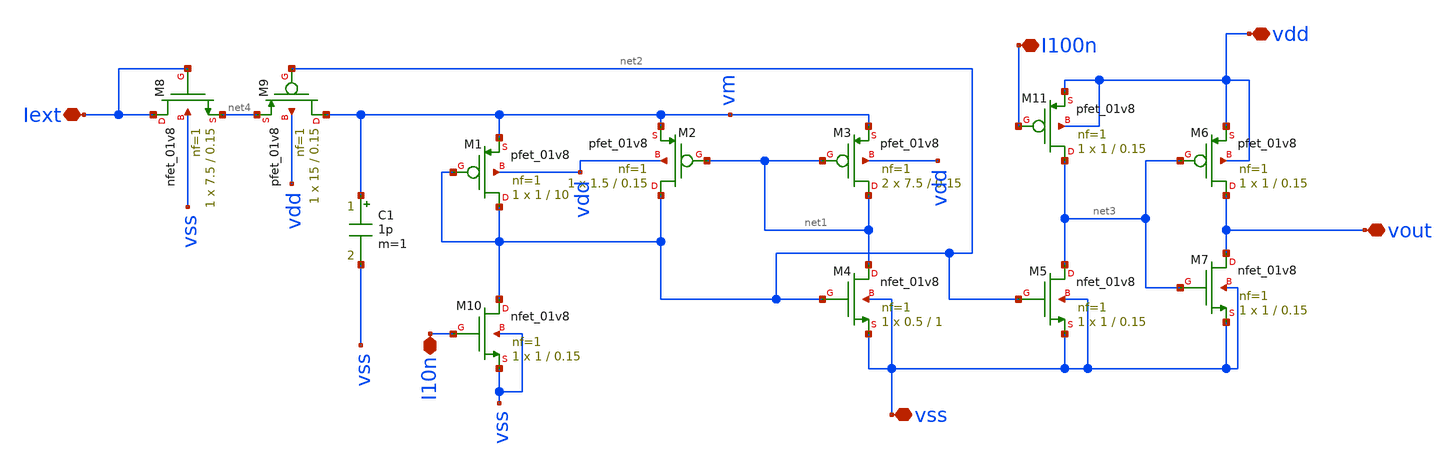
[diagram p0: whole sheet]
** sch_path: Neuron/ultralif/ultralif_res.sch
**.subckt ultralif_res Iext vout vss I10n vdd I100n
*.iopin Iext
*.iopin vout
*.iopin vss
*.iopin I10n
*.iopin vdd
*.iopin I100n
XM1 net2 net2 vm vdd sky130_fd_pr__pfet_01v8 L=10 W=1 nf=1 ad='int((nf+1)/2) * W/nf * 0.29' as='int((nf+2)/2) * W/nf * 0.29'
+ pd='2*int((nf+1)/2) * (W/nf + 0.29)' ps='2*int((nf+2)/2) * (W/nf + 0.29)' nrd='0.29 / W' nrs='0.29 / W'
+ sa=0 sb=0 sd=0 mult=1 m=1
XM2 net2 net1 vm vdd sky130_fd_pr__pfet_01v8 L=0.15 W=1.5 nf=1 ad='int((nf+1)/2) * W/nf * 0.29' as='int((nf+2)/2) * W/nf * 0.29'
+ pd='2*int((nf+1)/2) * (W/nf + 0.29)' ps='2*int((nf+2)/2) * (W/nf + 0.29)' nrd='0.29 / W' nrs='0.29 / W'
+ sa=0 sb=0 sd=0 mult=1 m=1
XM3 net1 net1 vm vdd sky130_fd_pr__pfet_01v8 L=0.15 W=7.5 nf=1 ad='int((nf+1)/2) * W/nf * 0.29' as='int((nf+2)/2) * W/nf * 0.29'
+ pd='2*int((nf+1)/2) * (W/nf + 0.29)' ps='2*int((nf+2)/2) * (W/nf + 0.29)' nrd='0.29 / W' nrs='0.29 / W'
+ sa=0 sb=0 sd=0 mult=2 m=2
XM4 net1 net2 vss vss sky130_fd_pr__nfet_01v8 L=1 W=0.5 nf=1 ad='int((1 + 1)/2) * 0.5 / 1 * 0.29' as='int((1 + 2)/2) * 0.5 / 1 * 0.29'
+ pd='2*int((1 + 1)/2) * (0.5 / 1 + 0.29)' ps='2*int((1 + 2)/2) * (0.5 / 1 + 0.29)' nrd='0.29 / 0.5 ' nrs='0.29 / 0.5 '
+ sa=0 sb=0 sd=0 mult=1 m=1
XM5 net3 net2 vss vss sky130_fd_pr__nfet_01v8 L=0.15 W=1 nf=1 ad='int((1 + 1)/2) * 1 / 1 * 0.29' as='int((1 + 2)/2) * 1 / 1 * 0.29'
+ pd='2*int((1 + 1)/2) * (1 / 1 + 0.29)' ps='2*int((1 + 2)/2) * (1 / 1 + 0.29)' nrd='0.29 / 1 ' nrs='0.29 / 1 '
+ sa=0 sb=0 sd=0 mult=1 m=1
XM6 vout net3 vdd vdd sky130_fd_pr__pfet_01v8 L=0.15 W=1 nf=1 ad='int((nf+1)/2) * W/nf * 0.29' as='int((nf+2)/2) * W/nf * 0.29'
+ pd='2*int((nf+1)/2) * (W/nf + 0.29)' ps='2*int((nf+2)/2) * (W/nf + 0.29)' nrd='0.29 / W' nrs='0.29 / W'
+ sa=0 sb=0 sd=0 mult=1 m=1
XM7 vout net3 vss vss sky130_fd_pr__nfet_01v8 L=0.15 W=1 nf=1 ad='int((1 + 1)/2) * 1 / 1 * 0.29' as='int((1 + 2)/2) * 1 / 1 * 0.29'
+ pd='2*int((1 + 1)/2) * (1 / 1 + 0.29)' ps='2*int((1 + 2)/2) * (1 / 1 + 0.29)' nrd='0.29 / 1 ' nrs='0.29 / 1 '
+ sa=0 sb=0 sd=0 mult=1 m=1
C1 vm vss 1p m=1
XM9 vm net2 net4 vdd sky130_fd_pr__pfet_01v8 L=0.15 W=15 nf=1 ad='int((nf+1)/2) * W/nf * 0.29' as='int((nf+2)/2) * W/nf * 0.29'
+ pd='2*int((nf+1)/2) * (W/nf + 0.29)' ps='2*int((nf+2)/2) * (W/nf + 0.29)' nrd='0.29 / W' nrs='0.29 / W'
+ sa=0 sb=0 sd=0 mult=1 m=1
XM8 Iext Iext net4 vss sky130_fd_pr__nfet_01v8 L=0.15 W=7.5 nf=1 ad='int((1 + 1)/2) * 7.5 / 1 * 0.29'
+ as='int((1 + 2)/2) * 7.5 / 1 * 0.29' pd='2*int((1 + 1)/2) * (7.5 / 1 + 0.29)' ps='2*int((1 + 2)/2) * (7.5 / 1 + 0.29)'
+ nrd='0.29 / 7.5 ' nrs='0.29 / 7.5 ' sa=0 sb=0 sd=0 mult=1 m=1
XM10 net2 I10n vss vss sky130_fd_pr__nfet_01v8 L=0.15 W=1 nf=1 ad='int((1 + 1)/2) * 1 / 1 * 0.29' as='int((1 + 2)/2) * 1 / 1 * 0.29'
+ pd='2*int((1 + 1)/2) * (1 / 1 + 0.29)' ps='2*int((1 + 2)/2) * (1 / 1 + 0.29)' nrd='0.29 / 1 ' nrs='0.29 / 1 '
+ sa=0 sb=0 sd=0 mult=1 m=1
XM11 net3 I100n vdd vdd sky130_fd_pr__pfet_01v8 L=0.15 W=1 nf=1 ad='int((nf+1)/2) * W/nf * 0.29' as='int((nf+2)/2) * W/nf * 0.29'
+ pd='2*int((nf+1)/2) * (W/nf + 0.29)' ps='2*int((nf+2)/2) * (W/nf + 0.29)' nrd='0.29 / W' nrs='0.29 / W'
+ sa=0 sb=0 sd=0 mult=1 m=1
**.ends
.end
